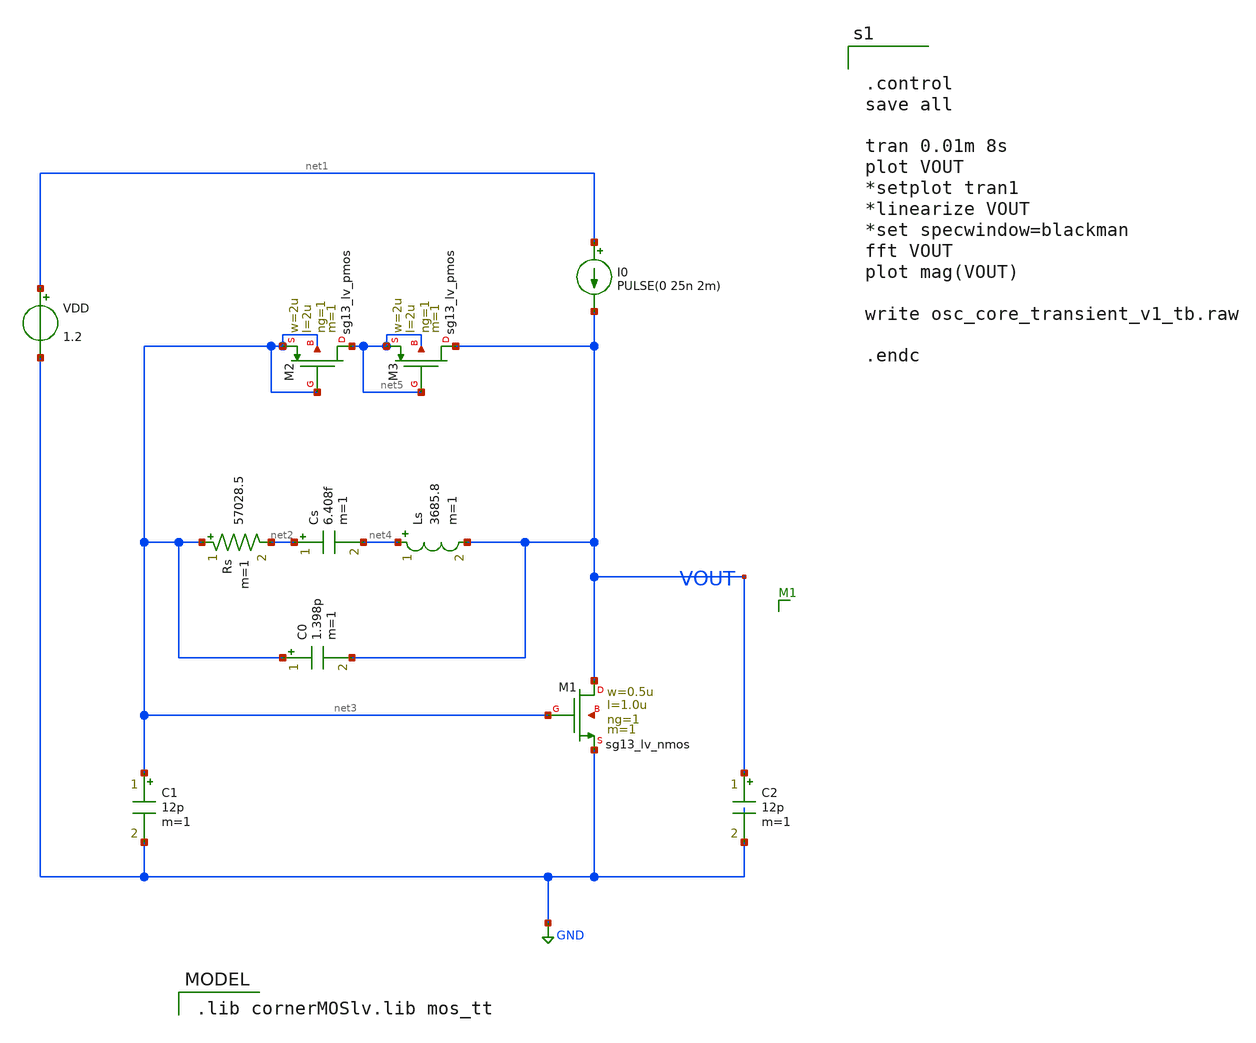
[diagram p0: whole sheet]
** sch_path: osc_core_transient_v1_tb.sch
**.subckt osc_core_transient_v1_tb
XM1 VOUT net3 GND net6 sg13_lv_nmos w=0.5u l=1.0u ng=1 m=1 mm_ok=1
C1 net3 GND 12p m=1
C2 VOUT GND 12p m=1
I0 net1 VOUT PULSE(0 25n 2m)
Rs net3 net2 57028.5 m=1
Cs net2 net4 6.408f m=1
C0 net3 VOUT 1.398p m=1
Ls net4 VOUT 3685.8 m=1
VDD net1 GND 1.2
XM2 net5 net3 net3 net3 sg13_lv_pmos w=2u l=2u ng=1 m=1 mm_ok=1
XM3 VOUT net5 net5 net5 sg13_lv_pmos w=2u l=2u ng=1 m=1 mm_ok=1
**** begin user architecture code


.control
save all

tran 0.01m 8s
plot VOUT
*setplot tran1
*linearize VOUT
*set specwindow=blackman
fft VOUT
plot mag(VOUT)

write osc_core_transient_v1_tb.raw

.endc


 .lib cornerMOSlv.lib mos_tt

**** end user architecture code
**.ends
.GLOBAL GND
.end
